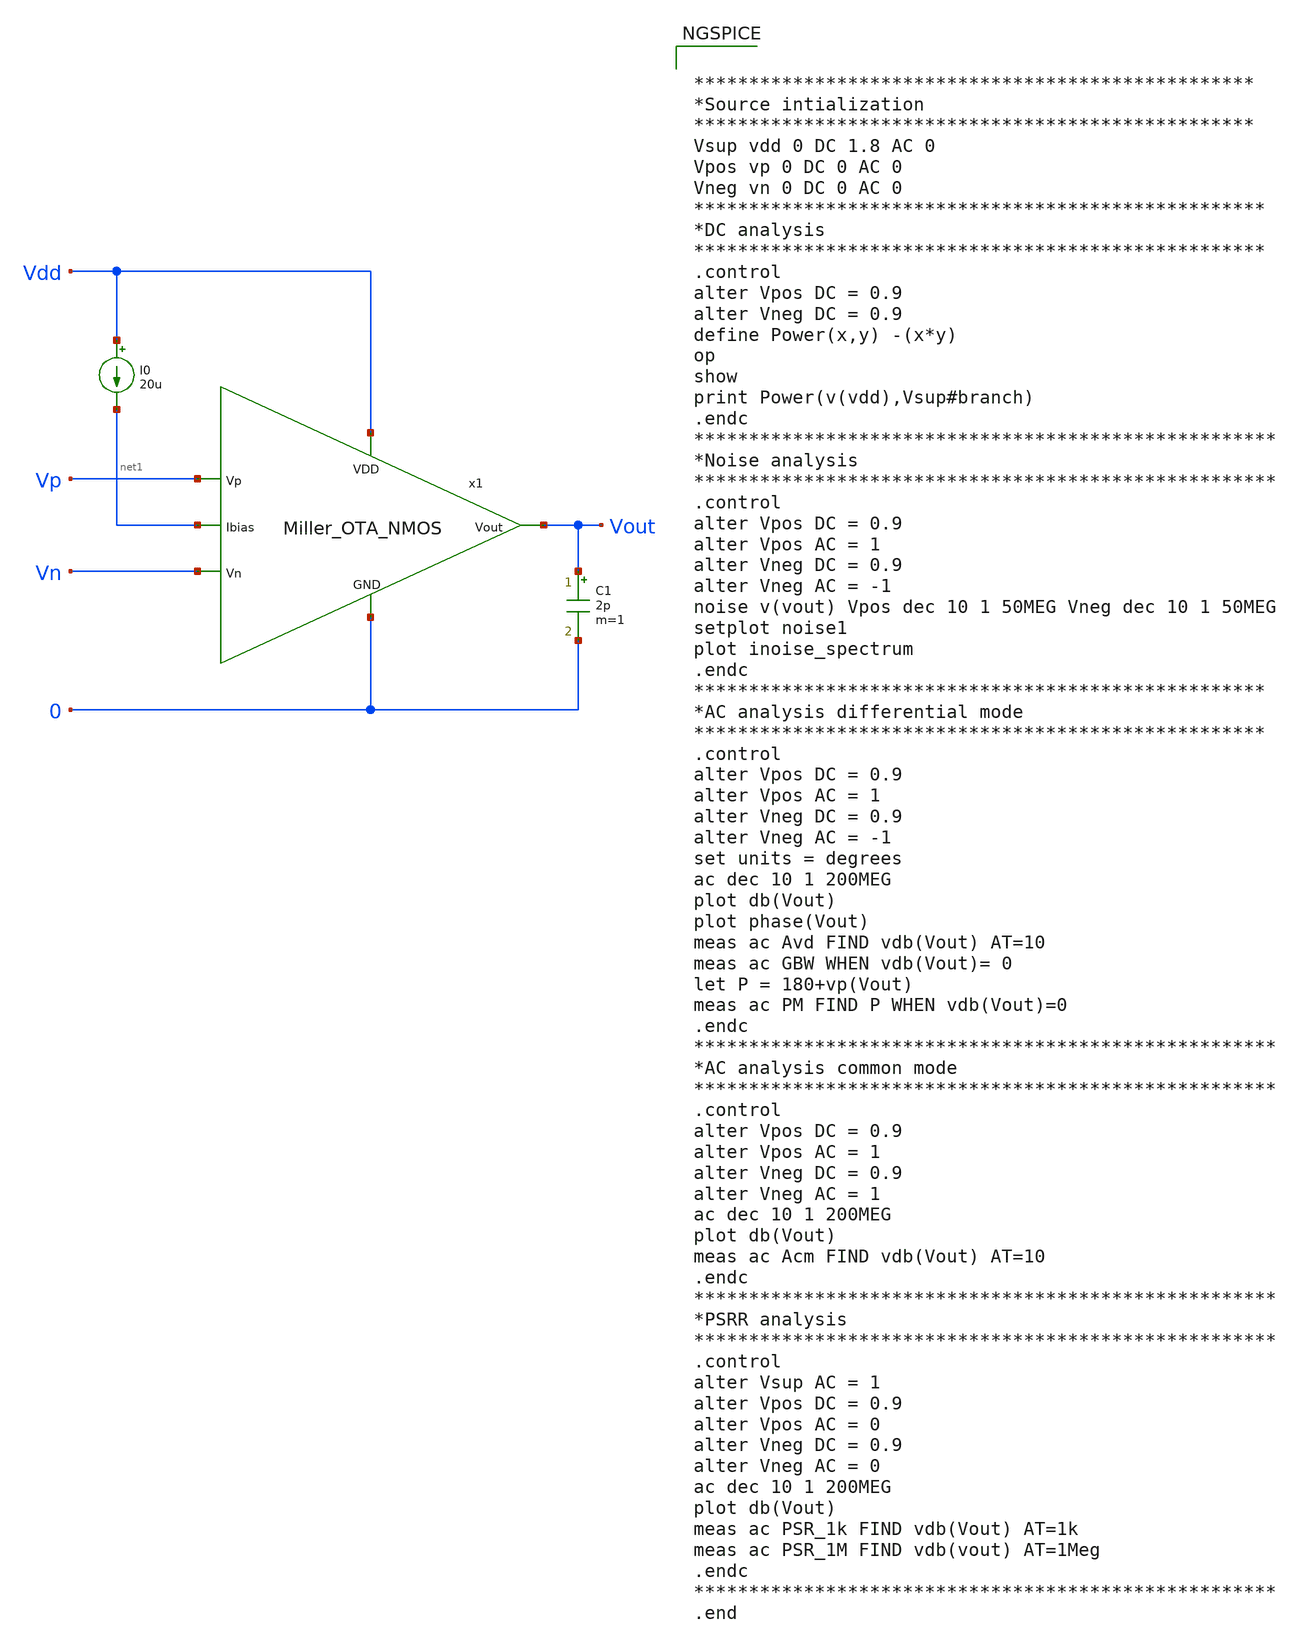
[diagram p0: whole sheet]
** sch_path: Analog_Blocks/OTA/Testbench/Miller_OTA/Transistor5v/Miller_OTA5v_meas.sch
**.subckt Miller_OTA5v_meas
I0 Vdd net1 20u
C1 Vout 0 2p m=1
x1 Vdd Vn Vp Vout net1 0 Miller_OTA_NMOS
**** begin user architecture code

.include ~/Analog_blocks/models/skywater-pdk/libraries/sky130_fd_pr/latest/cells/nfet_01v8/sky130_fd_pr__nfet_01v8__tt.corner.spice
.include ~/Analog_blocks/models/skywater-pdk/libraries/sky130_fd_pr/latest/cells/nfet_01v8_lvt/sky130_fd_pr__nfet_01v8_lvt__tt.corner.spice
.include ~/Analog_blocks/models/skywater-pdk/libraries/sky130_fd_pr/latest/cells/pfet_01v8/sky130_fd_pr__pfet_01v8__tt.corner.spice
.include ~/Analog_blocks/models/skywater-pdk/libraries/sky130_fd_pr/latest/cells/nfet_03v3_nvt/sky130_fd_pr__nfet_03v3_nvt__tt.corner.spice
.include ~/Analog_blocks/models/skywater-pdk/libraries/sky130_fd_pr/latest/cells/nfet_05v0_nvt/sky130_fd_pr__nfet_05v0_nvt__tt.corner.spice
.include ~/Analog_blocks/models/skywater-pdk/libraries/sky130_fd_pr/latest/cells/esd_nfet_01v8/sky130_fd_pr__esd_nfet_01v8__tt.corner.spice
.include ~/Analog_blocks/models/skywater-pdk/libraries/sky130_fd_pr/latest/cells/pfet_01v8_lvt/sky130_fd_pr__pfet_01v8_lvt__tt.corner.spice
.include ~/Analog_blocks/models/skywater-pdk/libraries/sky130_fd_pr/latest/cells/pfet_01v8_hvt/sky130_fd_pr__pfet_01v8_hvt__tt.corner.spice
.include ~/Analog_blocks/models/skywater-pdk/libraries/sky130_fd_pr/latest/cells/esd_pfet_g5v0d10v5/sky130_fd_pr__esd_pfet_g5v0d10v5__tt.corner.spice
.include ~/Analog_blocks/models/skywater-pdk/libraries/sky130_fd_pr/latest/cells/pfet_g5v0d10v5/sky130_fd_pr__pfet_g5v0d10v5__tt.corner.spice
.include ~/Analog_blocks/models/skywater-pdk/libraries/sky130_fd_pr/latest/cells/pfet_g5v0d16v0/sky130_fd_pr__pfet_g5v0d16v0__tt.corner.spice
.include ~/Analog_blocks/models/skywater-pdk/libraries/sky130_fd_pr/latest/cells/nfet_g5v0d10v5/sky130_fd_pr__nfet_g5v0d10v5__tt.corner.spice
.include ~/Analog_blocks/models/skywater-pdk/libraries/sky130_fd_pr/latest/cells/nfet_g5v0d16v0/sky130_fd_pr__nfet_g5v0d16v0__tt_discrete.corner.spice
.include ~/Analog_blocks/models/skywater-pdk/libraries/sky130_fd_pr/latest/cells/esd_nfet_g5v0d10v5/sky130_fd_pr__esd_nfet_g5v0d10v5__tt.corner.spice
.include ~/Analog_blocks/models/skywater-pdk/libraries/sky130_fd_pr/latest/models/corners/tt/nonfet.spice
* Mismatch parameters
.include ~/Analog_blocks/models/skywater-pdk/libraries/sky130_fd_pr/latest/cells/nfet_01v8/sky130_fd_pr__nfet_01v8__mismatch.corner.spice
.include ~/Analog_blocks/models/skywater-pdk/libraries/sky130_fd_pr/latest/cells/pfet_01v8/sky130_fd_pr__pfet_01v8__mismatch.corner.spice
.include ~/Analog_blocks/models/skywater-pdk/libraries/sky130_fd_pr/latest/cells/nfet_01v8_lvt/sky130_fd_pr__nfet_01v8_lvt__mismatch.corner.spice
.include ~/Analog_blocks/models/skywater-pdk/libraries/sky130_fd_pr/latest/cells/pfet_01v8_lvt/sky130_fd_pr__pfet_01v8_lvt__mismatch.corner.spice
.include ~/Analog_blocks/models/skywater-pdk/libraries/sky130_fd_pr/latest/cells/pfet_01v8_hvt/sky130_fd_pr__pfet_01v8_hvt__mismatch.corner.spice
.include ~/Analog_blocks/models/skywater-pdk/libraries/sky130_fd_pr/latest/cells/nfet_g5v0d10v5/sky130_fd_pr__nfet_g5v0d10v5__mismatch.corner.spice
.include ~/Analog_blocks/models/skywater-pdk/libraries/sky130_fd_pr/latest/cells/pfet_g5v0d10v5/sky130_fd_pr__pfet_g5v0d10v5__mismatch.corner.spice
.include ~/Analog_blocks/models/skywater-pdk/libraries/sky130_fd_pr/latest/cells/nfet_05v0_nvt/sky130_fd_pr__nfet_05v0_nvt__mismatch.corner.spice
.include ~/Analog_blocks/models/skywater-pdk/libraries/sky130_fd_pr/latest/cells/nfet_03v3_nvt/sky130_fd_pr__nfet_03v3_nvt__mismatch.corner.spice
* Resistor
.include ~/Analog_blocks/models/skywater-pdk/libraries/sky130_fd_pr/latest/models/r+c/res_typical__cap_typical.spice
.include ~/Analog_blocks/models/skywater-pdk/libraries/sky130_fd_pr/latest/models/r+c/res_typical__cap_typical__lin.spice
* Special cells
.include ~/Analog_blocks/models/skywater-pdk/libraries/sky130_fd_pr/latest/models/corners/tt/specialized_cells.spice
* All models
.include ~/Analog_blocks/models/skywater-pdk/libraries/sky130_fd_pr/latest/models/all.spice
* Corner
.include ~/Analog_blocks/models/skywater-pdk/libraries/sky130_fd_pr/latest/models/corners/tt/rf.spice



***************************************************
*Source intialization
***************************************************
Vsup vdd 0 DC 1.8 AC 0
Vpos vp 0 DC 0 AC 0
Vneg vn 0 DC 0 AC 0
****************************************************
*DC analysis
****************************************************
.control
alter Vpos DC = 0.9
alter Vneg DC = 0.9
define Power(x,y) -(x*y)
op
show
print Power(v(vdd),Vsup#branch)
.endc
*****************************************************
*Noise analysis
*****************************************************
.control
alter Vpos DC = 0.9
alter Vpos AC = 1
alter Vneg DC = 0.9
alter Vneg AC = -1
noise v(vout) Vpos dec 10 1 50MEG Vneg dec 10 1 50MEG
setplot noise1
plot inoise_spectrum
.endc
****************************************************
*AC analysis differential mode
****************************************************
.control
alter Vpos DC = 0.9
alter Vpos AC = 1
alter Vneg DC = 0.9
alter Vneg AC = -1
set units = degrees
ac dec 10 1 200MEG
plot db(Vout)
plot phase(Vout)
meas ac Avd FIND vdb(Vout) AT=10
meas ac GBW WHEN vdb(Vout)= 0
let P = 180+vp(Vout)
meas ac PM FIND P WHEN vdb(Vout)=0
.endc
*****************************************************
*AC analysis common mode
*****************************************************
.control
alter Vpos DC = 0.9
alter Vpos AC = 1
alter Vneg DC = 0.9
alter Vneg AC = 1
ac dec 10 1 200MEG
plot db(Vout)
meas ac Acm FIND vdb(Vout) AT=10
.endc
*****************************************************
*PSRR analysis
*****************************************************
.control
alter Vsup AC = 1
alter Vpos DC = 0.9
alter Vpos AC = 0
alter Vneg DC = 0.9
alter Vneg AC = 0
ac dec 10 1 200MEG
plot db(Vout)
meas ac PSR_1k FIND vdb(Vout) AT=1k
meas ac PSR_1M FIND vdb(vout) AT=1Meg
.endc
*****************************************************
.end


**** end user architecture code
**.ends

* expanding   symbol:
*+  /home/eslam/Analog_blocks/Analog_Blocks/OTA/Schematic/Miller_OTA/Transistor5v/Miller_OTA_NMOS.sym # of pins=6
** sym_path: Analog_Blocks/OTA/Schematic/Miller_OTA/Transistor5v/Miller_OTA_NMOS.sym
** sch_path: Analog_Blocks/OTA/Schematic/Miller_OTA/Transistor5v/Miller_OTA_NMOS.sch
.subckt Miller_OTA_NMOS VDD Vn Vp Vout Ibias GND
*.ipin VDD
*.ipin Ibias
*.ipin Vn
*.ipin Vp
*.opin Vout
*.ipin GND
XM1 net1 Vn net3 GND sky130_fd_pr__nfet_g5v0d10v5 L=0.5 W=10 nf=1 ad='int((nf+1)/2) * W/nf * 0.29' as='int((nf+2)/2) * W/nf * 0.29'
+ pd='2*int((nf+1)/2) * (W/nf + 0.29)' ps='2*int((nf+2)/2) * (W/nf + 0.29)' nrd='0.29 / W' nrs='0.29 / W'
+ sa=0 sb=0 sd=0 mult=8 m=8
XM2 net2 Vp net3 GND sky130_fd_pr__nfet_g5v0d10v5 L=0.5 W=10 nf=1 ad='int((nf+1)/2) * W/nf * 0.29' as='int((nf+2)/2) * W/nf * 0.29'
+ pd='2*int((nf+1)/2) * (W/nf + 0.29)' ps='2*int((nf+2)/2) * (W/nf + 0.29)' nrd='0.29 / W' nrs='0.29 / W'
+ sa=0 sb=0 sd=0 mult=8 m=8
XM3 net1 net1 VDD VDD sky130_fd_pr__pfet_g5v0d10v5 L=0.5 W=5 nf=1 ad='int((nf+1)/2) * W/nf * 0.29' as='int((nf+2)/2) * W/nf * 0.29'
+ pd='2*int((nf+1)/2) * (W/nf + 0.29)' ps='2*int((nf+2)/2) * (W/nf + 0.29)' nrd='0.29 / W' nrs='0.29 / W'
+ sa=0 sb=0 sd=0 mult=4 m=4
XM4 net2 net1 VDD VDD sky130_fd_pr__pfet_g5v0d10v5 L=0.5 W=5 nf=1 ad='int((nf+1)/2) * W/nf * 0.29' as='int((nf+2)/2) * W/nf * 0.29'
+ pd='2*int((nf+1)/2) * (W/nf + 0.29)' ps='2*int((nf+2)/2) * (W/nf + 0.29)' nrd='0.29 / W' nrs='0.29 / W'
+ sa=0 sb=0 sd=0 mult=4 m=4
XM6 Vout net2 VDD VDD sky130_fd_pr__pfet_g5v0d10v5 L=0.5 W=5 nf=1 ad='int((nf+1)/2) * W/nf * 0.29' as='int((nf+2)/2) * W/nf * 0.29'
+ pd='2*int((nf+1)/2) * (W/nf + 0.29)' ps='2*int((nf+2)/2) * (W/nf + 0.29)' nrd='0.29 / W' nrs='0.29 / W'
+ sa=0 sb=0 sd=0 mult=20 m=20
XM5 net3 Ibias GND GND sky130_fd_pr__nfet_g5v0d10v5 L=1 W=3 nf=1 ad='int((nf+1)/2) * W/nf * 0.29' as='int((nf+2)/2) * W/nf * 0.29'
+ pd='2*int((nf+1)/2) * (W/nf + 0.29)' ps='2*int((nf+2)/2) * (W/nf + 0.29)' nrd='0.29 / W' nrs='0.29 / W'
+ sa=0 sb=0 sd=0 mult=8 m=8
XM8 Ibias Ibias GND GND sky130_fd_pr__nfet_g5v0d10v5 L=1 W=3 nf=1 ad='int((nf+1)/2) * W/nf * 0.29' as='int((nf+2)/2) * W/nf * 0.29'
+ pd='2*int((nf+1)/2) * (W/nf + 0.29)' ps='2*int((nf+2)/2) * (W/nf + 0.29)' nrd='0.29 / W' nrs='0.29 / W'
+ sa=0 sb=0 sd=0 mult=8 m=8
XC1 net2 Vout sky130_fd_pr__cap_mim_m3_2 W=25 L=25 MF=1 m=1
XM7 Vout Ibias GND GND sky130_fd_pr__nfet_g5v0d10v5 L=1 W=3 nf=1 ad='int((nf+1)/2) * W/nf * 0.29' as='int((nf+2)/2) * W/nf * 0.29'
+ pd='2*int((nf+1)/2) * (W/nf + 0.29)' ps='2*int((nf+2)/2) * (W/nf + 0.29)' nrd='0.29 / W' nrs='0.29 / W'
+ sa=0 sb=0 sd=0 mult=16 m=16
.ends

.end
